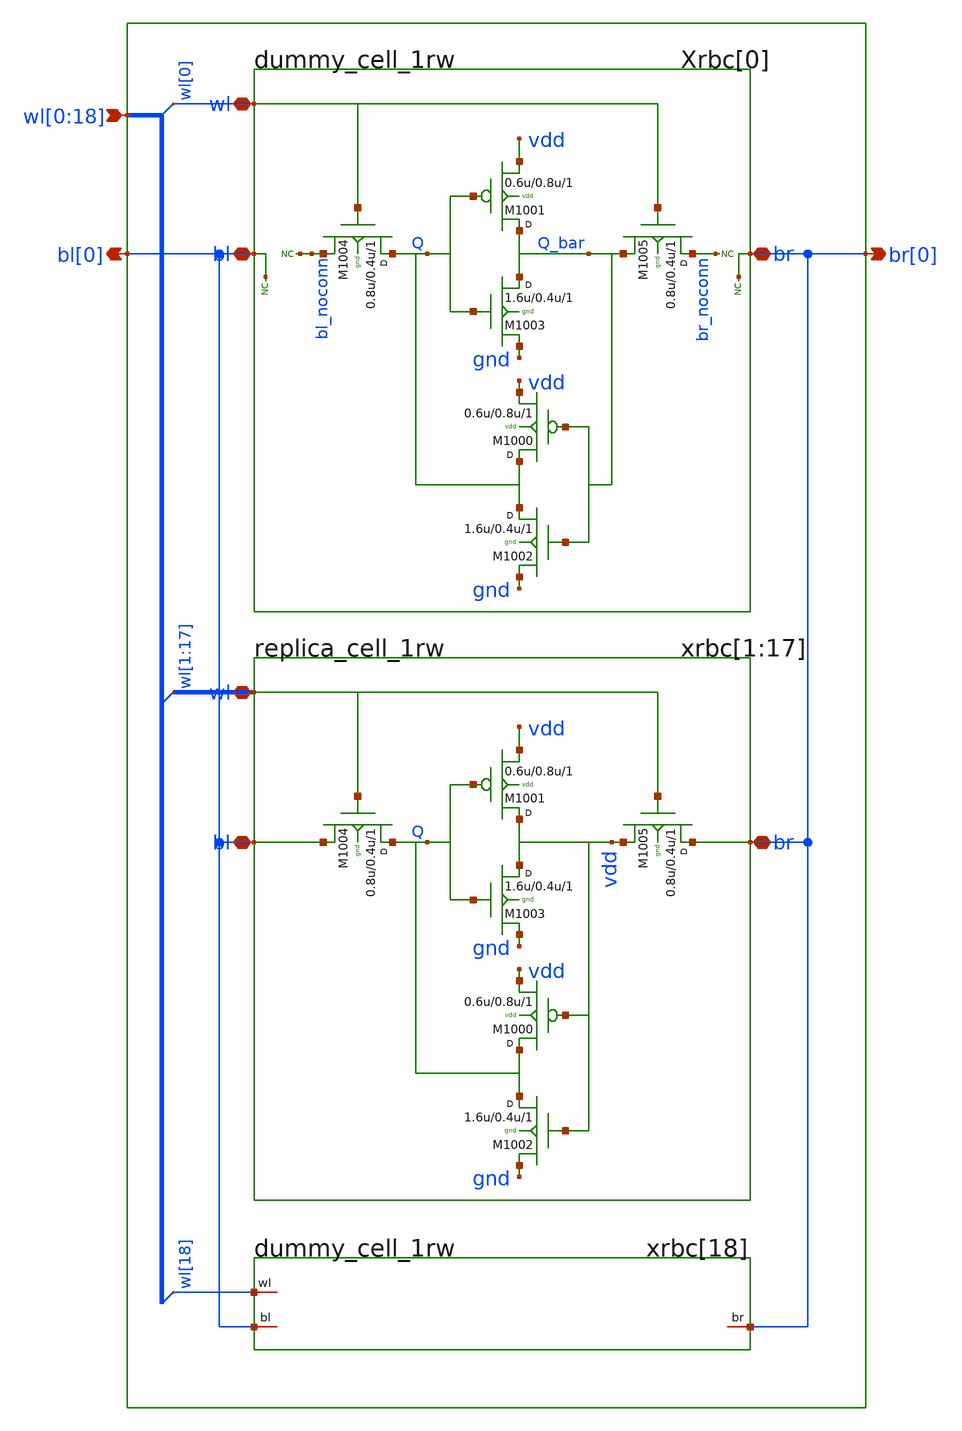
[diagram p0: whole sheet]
** sch_path: sram_4_16_scn4m/replica_column.sch
**.subckt replica_column bl[0] br[0]
*+ wl[0],wl[1],wl[2],wl[3],wl[4],wl[5],wl[6],wl[7],wl[8],wl[9],wl[10],wl[11],wl[12],wl[13],wl[14],wl[15],wl[16],wl[17],wl[18]
*.opin bl[0]
*.opin br[0]
*.ipin
*+ wl[0],wl[1],wl[2],wl[3],wl[4],wl[5],wl[6],wl[7],wl[8],wl[9],wl[10],wl[11],wl[12],wl[13],wl[14],wl[15],wl[16],wl[17],wl[18]
Xrbc[0] bl[0] br[0] wl[0] vdd gnd dummy_cell_1rw
xrbc[1] bl[0] br[0] wl[1] vdd gnd replica_cell_1rw
xrbc[2] bl[0] br[0] wl[2] vdd gnd replica_cell_1rw
xrbc[3] bl[0] br[0] wl[3] vdd gnd replica_cell_1rw
xrbc[4] bl[0] br[0] wl[4] vdd gnd replica_cell_1rw
xrbc[5] bl[0] br[0] wl[5] vdd gnd replica_cell_1rw
xrbc[6] bl[0] br[0] wl[6] vdd gnd replica_cell_1rw
xrbc[7] bl[0] br[0] wl[7] vdd gnd replica_cell_1rw
xrbc[8] bl[0] br[0] wl[8] vdd gnd replica_cell_1rw
xrbc[9] bl[0] br[0] wl[9] vdd gnd replica_cell_1rw
xrbc[10] bl[0] br[0] wl[10] vdd gnd replica_cell_1rw
xrbc[11] bl[0] br[0] wl[11] vdd gnd replica_cell_1rw
xrbc[12] bl[0] br[0] wl[12] vdd gnd replica_cell_1rw
xrbc[13] bl[0] br[0] wl[13] vdd gnd replica_cell_1rw
xrbc[14] bl[0] br[0] wl[14] vdd gnd replica_cell_1rw
xrbc[15] bl[0] br[0] wl[15] vdd gnd replica_cell_1rw
xrbc[16] bl[0] br[0] wl[16] vdd gnd replica_cell_1rw
xrbc[17] bl[0] br[0] wl[17] vdd gnd replica_cell_1rw
xrbc[18] bl[0] br[0] wl[18] vdd gnd dummy_cell_1rw
**.ends

* expanding   symbol:  dummy_cell_1rw.sch # of pins=3
** sym_path: sram_4_16_scn4m/dummy_cell_1rw.sch
** sch_path: sram_4_16_scn4m/dummy_cell_1rw.sch
.subckt dummy_cell_1rw bl br wl vdd gnd
*.iopin bl
*.iopin br
*.iopin wl
M1004 Q wl bl_noconn gnd n w=0.8u l=0.4u m=1
M1001 Q_bar Q vdd vdd p w=0.6u l=0.8u m=1
M1003 Q_bar Q gnd gnd n w=1.6u l=0.4u m=1
M1002 Q Q_bar gnd gnd n w=1.6u l=0.4u m=1
M1000 Q Q_bar vdd vdd p w=0.6u l=0.8u m=1
M1005 br_noconn wl Q_bar gnd n w=0.8u l=0.4u m=1
* noconn bl_noconn
* noconn br_noconn
* noconn br
* noconn bl
.ends


* expanding   symbol:  replica_cell_1rw.sch # of pins=3
** sym_path: sram_4_16_scn4m/replica_cell_1rw.sch
** sch_path: sram_4_16_scn4m/replica_cell_1rw.sch
.subckt replica_cell_1rw bl br wl vdd gnd
*.iopin bl
*.iopin br
*.iopin wl
M1004 Q wl bl gnd n w=0.8u l=0.4u m=1
M1001 vdd Q vdd vdd p w=0.6u l=0.8u m=1
M1003 vdd Q gnd gnd n w=1.6u l=0.4u m=1
M1002 Q vdd gnd gnd n w=1.6u l=0.4u m=1
M1000 Q vdd vdd vdd p w=0.6u l=0.8u m=1
M1005 br wl vdd gnd n w=0.8u l=0.4u m=1
.ends

.end
